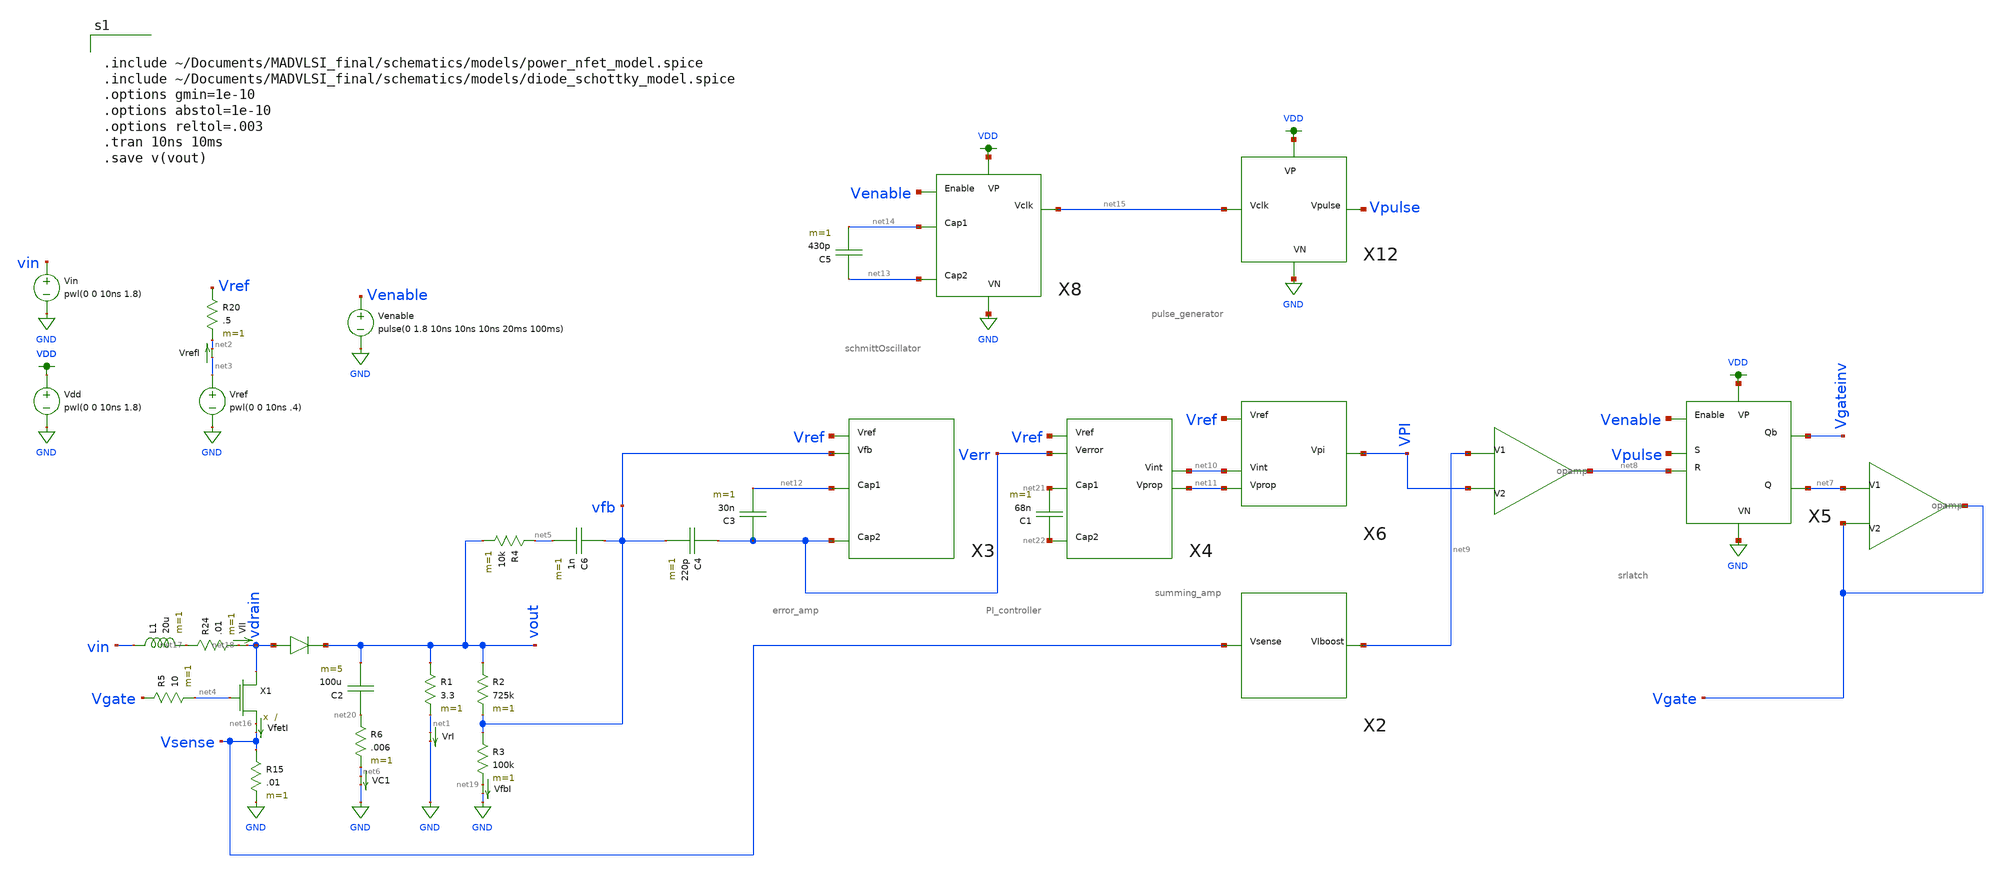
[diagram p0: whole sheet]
** sch_path: schematics/boost_controller.sch
**.subckt boost_controller
Vin vin GND pwl(0 0 10ns 1.8)
VfetI net16 Vsense 0
.save i(vfeti)
X1 vdrain net4 net16 power_nfet
L1 vin net17 20u m=1
D1 vdrain vout diode_schottky
R1 vout net1 3.3 m=1
VlI net18 vdrain 0
.save i(vli)
VrI net1 GND 0
.save i(vri)
R2 vout vfb 725k m=1
R3 vfb net19 100k m=1
Vdd VDD GND pwl(0 0 10ns 1.8)
Vref net3 GND pwl(0 0 10ns .4)
X11 net9 VPI net8 opamp
VrefI net3 net2 0
.save i(vrefi)
R24 net17 net18 .01 m=1
VfbI net19 GND 0
.save i(vfbi)
R20 Vref net2 .5 m=1
C3 Verr net12 30n m=1
C4 Verr vfb 220p m=1
R4 net5 vout 10k m=1
C6 vfb net5 1n m=1
R5 Vgate net4 10 m=1
C2 net20 vout 100u m=5
R6 net20 net6 .006 m=1
VC1 net6 GND 0
.save i(vc1)
R15 Vsense GND .01 m=1
X5 Venable Vpulse net8 VDD GND Vgateinv net7 srlatch
X10 net7 Vgate Vgate opamp
Venable Venable GND pulse(0 1.8 10ns 10ns 10ns 20ms 100ms)
X2 Vsense net9 current_boost
X3 Vref net12 vfb Verr error_amp
X4 Vref net21 Verr net22 net10 net11 PI_controller
C1 net22 net21 68n m=1
X6 Vref VPI net10 net11 summing_amp
X8 Venable net14 net13 VDD GND net15 schmittOscillator
C5 net13 net14 430p m=1
X12 Vpulse VDD GND net15 pulse_generator
**** begin user architecture code


.include ~/Documents/MADVLSI_final/schematics/models/power_nfet_model.spice
.include ~/Documents/MADVLSI_final/schematics/models/diode_schottky_model.spice
.options gmin=1e-10
.options abstol=1e-10
.options reltol=.003
.tran 10ns 10ms
.save v(vout)


.option wnflag=1
.lib ~/skywater/skywater-pdk/libraries/sky130_fd_pr_ngspice/latest/models/sky130.lib.spice tt

**** end user architecture code
**.ends
.GLOBAL GND
.GLOBAL VDD
.end
